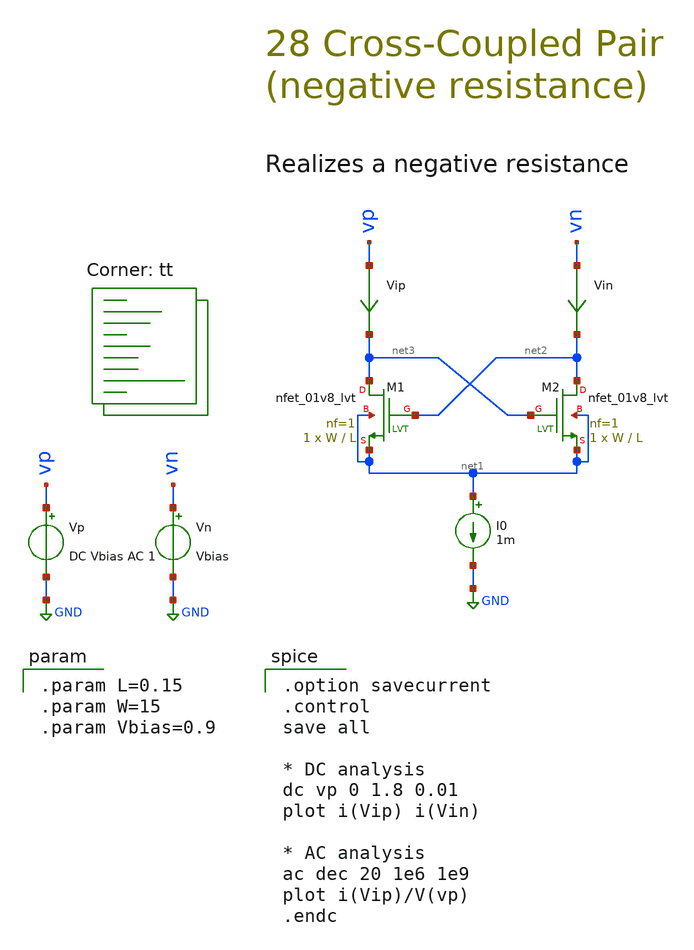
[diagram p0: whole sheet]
** sch_path: 28-a_cross-couple.sch
**.subckt 28-a_cross-couple
XM1 net3 net2 net1 net1 sky130_fd_pr__nfet_01v8_lvt L=L W=W nf=1 ad='int((1 + 1)/2) * W / 1 * 0.29' as='int((1 + 2)/2) * W / 1 * 0.29'
+ pd='2*int((1 + 1)/2) * (W / 1 + 0.29)' ps='2*int((1 + 2)/2) * (W / 1 + 0.29)' nrd='0.29 / W ' nrs='0.29 / W '
+ sa=0 sb=0 sd=0 mult=1 m=1
Vp vp GND DC Vbias AC 1
Vn vn GND Vbias
XM2 net2 net3 net1 net1 sky130_fd_pr__nfet_01v8_lvt L=L W=W nf=1 ad='int((1 + 1)/2) * W / 1 * 0.29' as='int((1 + 2)/2) * W / 1 * 0.29'
+ pd='2*int((1 + 1)/2) * (W / 1 + 0.29)' ps='2*int((1 + 2)/2) * (W / 1 + 0.29)' nrd='0.29 / W ' nrs='0.29 / W '
+ sa=0 sb=0 sd=0 mult=1 m=1
I0 net1 GND 1m
Vip vp net3 0
.save i(vip)
Vin vn net2 0
.save i(vin)
**** begin user architecture code
.lib $::SKYWATER_MODELS/sky130.lib.spice tt

.param L=0.15
.param W=15
.param Vbias=0.9


.option savecurrent
.control
save all

* DC analysis
dc vp 0 1.8 0.01
plot i(Vip) i(Vin)

* AC analysis
ac dec 20 1e6 1e9
plot i(Vip)/V(vp)
.endc

**** end user architecture code
**.ends
.GLOBAL GND
.end
